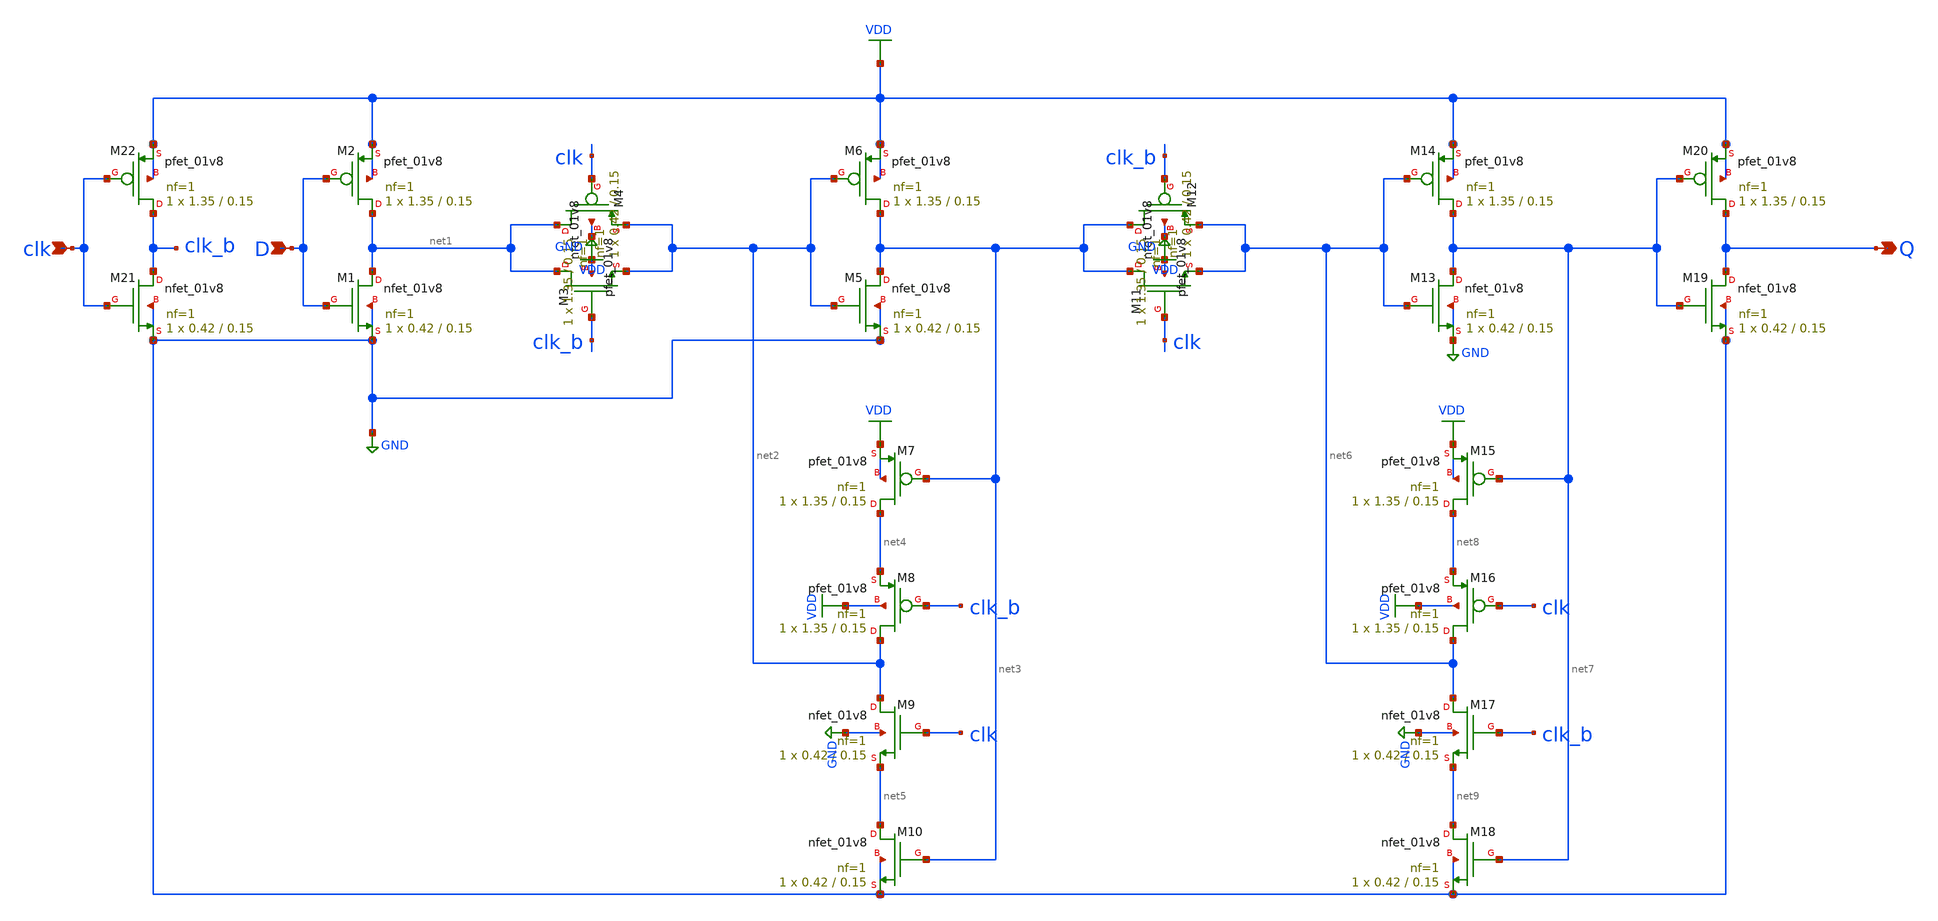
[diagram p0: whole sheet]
** sch_path: xschem/dff.sch
**.subckt dff D clk Q
*.ipin D
*.ipin clk
*.opin Q
XM1 net1 D GND GND sky130_fd_pr__nfet_01v8 L=0.15 W=0.42 nf=1 ad='int((nf+1)/2) * W/nf * 0.29' as='int((nf+2)/2) * W/nf * 0.29'
+ pd='2*int((nf+1)/2) * (W/nf + 0.29)' ps='2*int((nf+2)/2) * (W/nf + 0.29)' nrd='0.29 / W' nrs='0.29 / W'
+ sa=0 sb=0 sd=0 mult=1 m=1
XM2 net1 D VDD VDD sky130_fd_pr__pfet_01v8 L=0.15 W=1.35 nf=1 ad='int((nf+1)/2) * W/nf * 0.29' as='int((nf+2)/2) * W/nf * 0.29'
+ pd='2*int((nf+1)/2) * (W/nf + 0.29)' ps='2*int((nf+2)/2) * (W/nf + 0.29)' nrd='0.29 / W' nrs='0.29 / W'
+ sa=0 sb=0 sd=0 mult=1 m=1
XM3 net1 clk_b net2 GND sky130_fd_pr__nfet_01v8 L=0.15 W=0.42 nf=1 ad='int((nf+1)/2) * W/nf * 0.29' as='int((nf+2)/2) * W/nf * 0.29'
+ pd='2*int((nf+1)/2) * (W/nf + 0.29)' ps='2*int((nf+2)/2) * (W/nf + 0.29)' nrd='0.29 / W' nrs='0.29 / W'
+ sa=0 sb=0 sd=0 mult=1 m=1
XM4 net1 clk net2 VDD sky130_fd_pr__pfet_01v8 L=0.15 W=1.35 nf=1 ad='int((nf+1)/2) * W/nf * 0.29' as='int((nf+2)/2) * W/nf * 0.29'
+ pd='2*int((nf+1)/2) * (W/nf + 0.29)' ps='2*int((nf+2)/2) * (W/nf + 0.29)' nrd='0.29 / W' nrs='0.29 / W'
+ sa=0 sb=0 sd=0 mult=1 m=1
XM5 net3 net2 GND GND sky130_fd_pr__nfet_01v8 L=0.15 W=0.42 nf=1 ad='int((nf+1)/2) * W/nf * 0.29' as='int((nf+2)/2) * W/nf * 0.29'
+ pd='2*int((nf+1)/2) * (W/nf + 0.29)' ps='2*int((nf+2)/2) * (W/nf + 0.29)' nrd='0.29 / W' nrs='0.29 / W'
+ sa=0 sb=0 sd=0 mult=1 m=1
XM6 net3 net2 VDD VDD sky130_fd_pr__pfet_01v8 L=0.15 W=1.35 nf=1 ad='int((nf+1)/2) * W/nf * 0.29' as='int((nf+2)/2) * W/nf * 0.29'
+ pd='2*int((nf+1)/2) * (W/nf + 0.29)' ps='2*int((nf+2)/2) * (W/nf + 0.29)' nrd='0.29 / W' nrs='0.29 / W'
+ sa=0 sb=0 sd=0 mult=1 m=1
XM7 net4 net3 VDD VDD sky130_fd_pr__pfet_01v8 L=0.15 W=1.35 nf=1 ad='int((nf+1)/2) * W/nf * 0.29' as='int((nf+2)/2) * W/nf * 0.29'
+ pd='2*int((nf+1)/2) * (W/nf + 0.29)' ps='2*int((nf+2)/2) * (W/nf + 0.29)' nrd='0.29 / W' nrs='0.29 / W'
+ sa=0 sb=0 sd=0 mult=1 m=1
XM8 net2 clk_b net4 VDD sky130_fd_pr__pfet_01v8 L=0.15 W=1.35 nf=1 ad='int((nf+1)/2) * W/nf * 0.29' as='int((nf+2)/2) * W/nf * 0.29'
+ pd='2*int((nf+1)/2) * (W/nf + 0.29)' ps='2*int((nf+2)/2) * (W/nf + 0.29)' nrd='0.29 / W' nrs='0.29 / W'
+ sa=0 sb=0 sd=0 mult=1 m=1
XM9 net2 clk net5 GND sky130_fd_pr__nfet_01v8 L=0.15 W=0.42 nf=1 ad='int((nf+1)/2) * W/nf * 0.29' as='int((nf+2)/2) * W/nf * 0.29'
+ pd='2*int((nf+1)/2) * (W/nf + 0.29)' ps='2*int((nf+2)/2) * (W/nf + 0.29)' nrd='0.29 / W' nrs='0.29 / W'
+ sa=0 sb=0 sd=0 mult=1 m=1
XM10 net5 net3 GND GND sky130_fd_pr__nfet_01v8 L=0.15 W=0.42 nf=1 ad='int((nf+1)/2) * W/nf * 0.29' as='int((nf+2)/2) * W/nf * 0.29'
+ pd='2*int((nf+1)/2) * (W/nf + 0.29)' ps='2*int((nf+2)/2) * (W/nf + 0.29)' nrd='0.29 / W' nrs='0.29 / W'
+ sa=0 sb=0 sd=0 mult=1 m=1
XM11 net3 clk net6 GND sky130_fd_pr__nfet_01v8 L=0.15 W=0.42 nf=1 ad='int((nf+1)/2) * W/nf * 0.29' as='int((nf+2)/2) * W/nf * 0.29'
+ pd='2*int((nf+1)/2) * (W/nf + 0.29)' ps='2*int((nf+2)/2) * (W/nf + 0.29)' nrd='0.29 / W' nrs='0.29 / W'
+ sa=0 sb=0 sd=0 mult=1 m=1
XM12 net3 clk_b net6 VDD sky130_fd_pr__pfet_01v8 L=0.15 W=1.35 nf=1 ad='int((nf+1)/2) * W/nf * 0.29'
+ as='int((nf+2)/2) * W/nf * 0.29' pd='2*int((nf+1)/2) * (W/nf + 0.29)' ps='2*int((nf+2)/2) * (W/nf + 0.29)'
+ nrd='0.29 / W' nrs='0.29 / W' sa=0 sb=0 sd=0 mult=1 m=1
XM13 net7 net6 GND GND sky130_fd_pr__nfet_01v8 L=0.15 W=0.42 nf=1 ad='int((nf+1)/2) * W/nf * 0.29' as='int((nf+2)/2) * W/nf * 0.29'
+ pd='2*int((nf+1)/2) * (W/nf + 0.29)' ps='2*int((nf+2)/2) * (W/nf + 0.29)' nrd='0.29 / W' nrs='0.29 / W'
+ sa=0 sb=0 sd=0 mult=1 m=1
XM14 net7 net6 VDD VDD sky130_fd_pr__pfet_01v8 L=0.15 W=1.35 nf=1 ad='int((nf+1)/2) * W/nf * 0.29' as='int((nf+2)/2) * W/nf * 0.29'
+ pd='2*int((nf+1)/2) * (W/nf + 0.29)' ps='2*int((nf+2)/2) * (W/nf + 0.29)' nrd='0.29 / W' nrs='0.29 / W'
+ sa=0 sb=0 sd=0 mult=1 m=1
XM15 net8 net7 VDD VDD sky130_fd_pr__pfet_01v8 L=0.15 W=1.35 nf=1 ad='int((nf+1)/2) * W/nf * 0.29' as='int((nf+2)/2) * W/nf * 0.29'
+ pd='2*int((nf+1)/2) * (W/nf + 0.29)' ps='2*int((nf+2)/2) * (W/nf + 0.29)' nrd='0.29 / W' nrs='0.29 / W'
+ sa=0 sb=0 sd=0 mult=1 m=1
XM16 net6 clk net8 VDD sky130_fd_pr__pfet_01v8 L=0.15 W=1.35 nf=1 ad='int((nf+1)/2) * W/nf * 0.29' as='int((nf+2)/2) * W/nf * 0.29'
+ pd='2*int((nf+1)/2) * (W/nf + 0.29)' ps='2*int((nf+2)/2) * (W/nf + 0.29)' nrd='0.29 / W' nrs='0.29 / W'
+ sa=0 sb=0 sd=0 mult=1 m=1
XM17 net6 clk_b net9 GND sky130_fd_pr__nfet_01v8 L=0.15 W=0.42 nf=1 ad='int((nf+1)/2) * W/nf * 0.29'
+ as='int((nf+2)/2) * W/nf * 0.29' pd='2*int((nf+1)/2) * (W/nf + 0.29)' ps='2*int((nf+2)/2) * (W/nf + 0.29)'
+ nrd='0.29 / W' nrs='0.29 / W' sa=0 sb=0 sd=0 mult=1 m=1
XM18 net9 net7 GND GND sky130_fd_pr__nfet_01v8 L=0.15 W=0.42 nf=1 ad='int((nf+1)/2) * W/nf * 0.29' as='int((nf+2)/2) * W/nf * 0.29'
+ pd='2*int((nf+1)/2) * (W/nf + 0.29)' ps='2*int((nf+2)/2) * (W/nf + 0.29)' nrd='0.29 / W' nrs='0.29 / W'
+ sa=0 sb=0 sd=0 mult=1 m=1
XM19 Q net7 GND GND sky130_fd_pr__nfet_01v8 L=0.15 W=0.42 nf=1 ad='int((nf+1)/2) * W/nf * 0.29' as='int((nf+2)/2) * W/nf * 0.29'
+ pd='2*int((nf+1)/2) * (W/nf + 0.29)' ps='2*int((nf+2)/2) * (W/nf + 0.29)' nrd='0.29 / W' nrs='0.29 / W'
+ sa=0 sb=0 sd=0 mult=1 m=1
XM20 Q net7 VDD VDD sky130_fd_pr__pfet_01v8 L=0.15 W=1.35 nf=1 ad='int((nf+1)/2) * W/nf * 0.29' as='int((nf+2)/2) * W/nf * 0.29'
+ pd='2*int((nf+1)/2) * (W/nf + 0.29)' ps='2*int((nf+2)/2) * (W/nf + 0.29)' nrd='0.29 / W' nrs='0.29 / W'
+ sa=0 sb=0 sd=0 mult=1 m=1
XM21 clk_b clk GND GND sky130_fd_pr__nfet_01v8 L=0.15 W=0.42 nf=1 ad='int((nf+1)/2) * W/nf * 0.29' as='int((nf+2)/2) * W/nf * 0.29'
+ pd='2*int((nf+1)/2) * (W/nf + 0.29)' ps='2*int((nf+2)/2) * (W/nf + 0.29)' nrd='0.29 / W' nrs='0.29 / W'
+ sa=0 sb=0 sd=0 mult=1 m=1
XM22 clk_b clk VDD VDD sky130_fd_pr__pfet_01v8 L=0.15 W=1.35 nf=1 ad='int((nf+1)/2) * W/nf * 0.29' as='int((nf+2)/2) * W/nf * 0.29'
+ pd='2*int((nf+1)/2) * (W/nf + 0.29)' ps='2*int((nf+2)/2) * (W/nf + 0.29)' nrd='0.29 / W' nrs='0.29 / W'
+ sa=0 sb=0 sd=0 mult=1 m=1
**.ends
.GLOBAL GND
.GLOBAL VDD
.end
